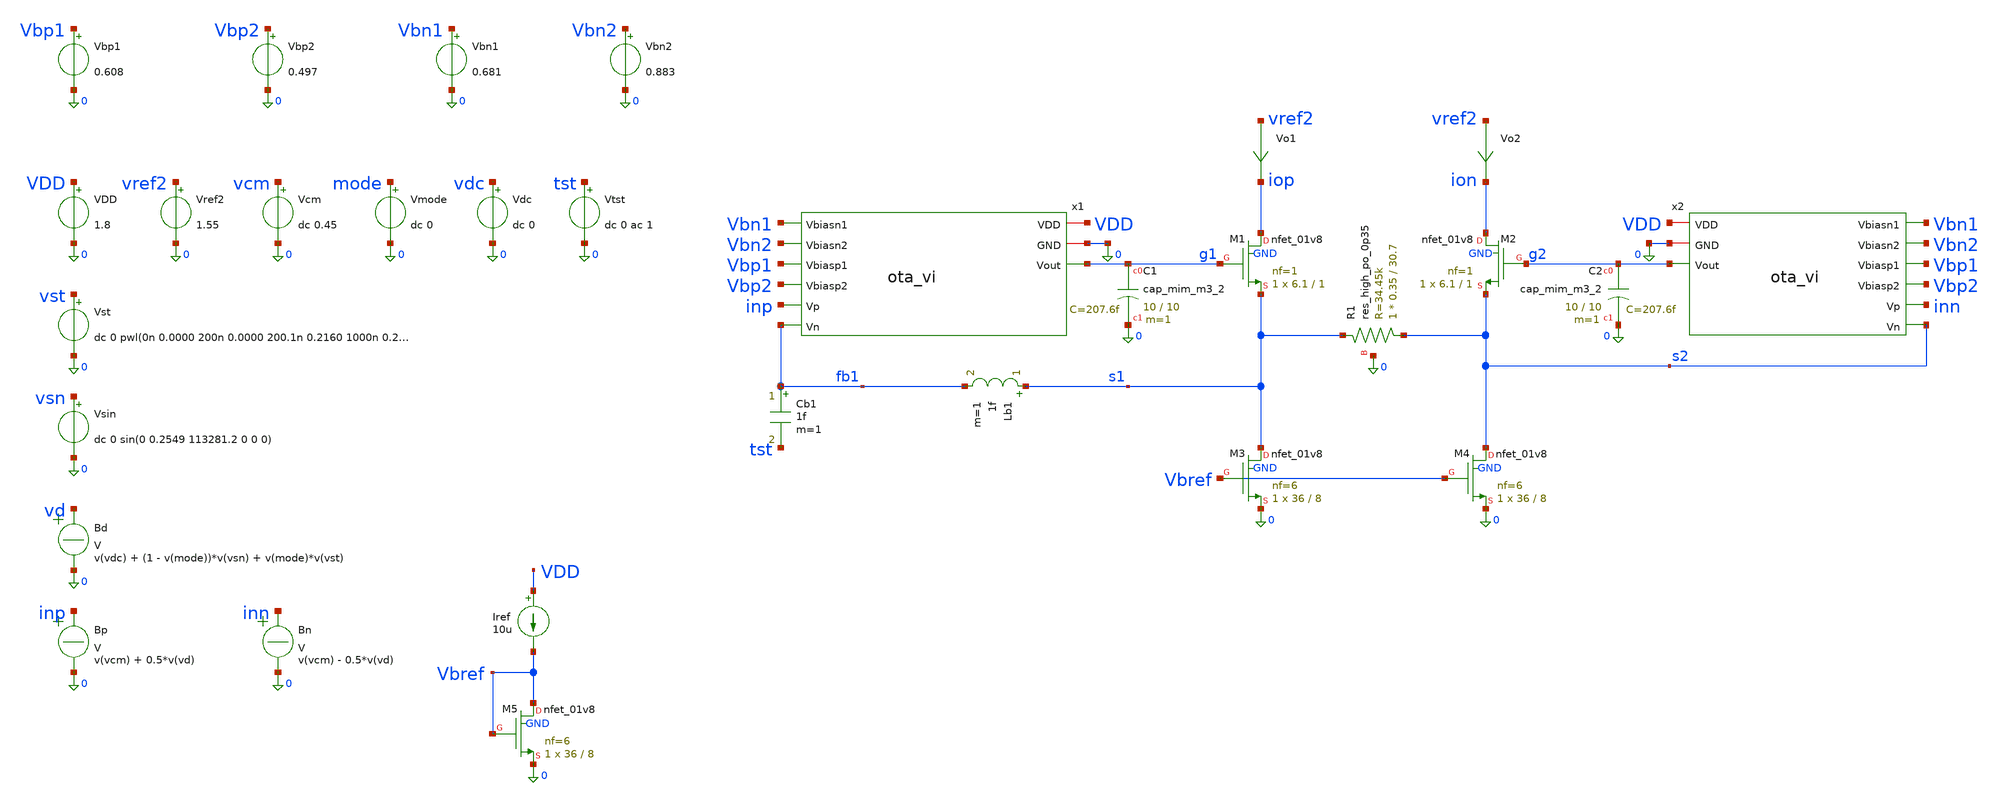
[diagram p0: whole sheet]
** sch_path: sch/vi_converter/vi_converter_tb.sch
**.subckt vi_converter_tb
x1 VDD 0 Vbn1 Vbn2 Vbp1 Vbp2 inp fb1 g1 ota_vi
XM1 iop g1 s1 GND sky130_fd_pr__nfet_01v8 L=1 W=6.1 nf=1 ad='int((1 + 1)/2) * 6.1 / 1 * 0.29' as='int((1 + 2)/2) * 6.1 / 1 * 0.29'
+ pd='2*int((1 + 1)/2) * (6.1 / 1 + 0.29)' ps='2*int((1 + 2)/2) * (6.1 / 1 + 0.29)' nrd='0.29 / 6.1 ' nrs='0.29 / 6.1 '
+ sa=0 sb=0 sd=0 mult=1 m=1
XM2 ion g2 s2 GND sky130_fd_pr__nfet_01v8 L=1 W=6.1 nf=1 ad='int((1 + 1)/2) * 6.1 / 1 * 0.29' as='int((1 + 2)/2) * 6.1 / 1 * 0.29'
+ pd='2*int((1 + 1)/2) * (6.1 / 1 + 0.29)' ps='2*int((1 + 2)/2) * (6.1 / 1 + 0.29)' nrd='0.29 / 6.1 ' nrs='0.29 / 6.1 '
+ sa=0 sb=0 sd=0 mult=1 m=1
XM3 s1 Vbref 0 GND sky130_fd_pr__nfet_01v8 L=8 W=36 nf=6 ad='int((6 + 1)/2) * 36 / 6 * 0.29' as='int((6 + 2)/2) * 36 / 6 * 0.29'
+ pd='2*int((6 + 1)/2) * (36 / 6 + 0.29)' ps='2*int((6 + 2)/2) * (36 / 6 + 0.29)' nrd='0.29 / 36 ' nrs='0.29 / 36 '
+ sa=0 sb=0 sd=0 mult=1 m=1
XM4 s2 Vbref 0 GND sky130_fd_pr__nfet_01v8 L=8 W=36 nf=6 ad='int((6 + 1)/2) * 36 / 6 * 0.29' as='int((6 + 2)/2) * 36 / 6 * 0.29'
+ pd='2*int((6 + 1)/2) * (36 / 6 + 0.29)' ps='2*int((6 + 2)/2) * (36 / 6 + 0.29)' nrd='0.29 / 36 ' nrs='0.29 / 36 '
+ sa=0 sb=0 sd=0 mult=1 m=1
VDD VDD 0 1.8
.save i(vdd)
Iref VDD Vbref 10u
XC1 g1 0 sky130_fd_pr__cap_mim_m3_2 W=10 L=10 MF=1 m=1
x2 VDD 0 Vbn1 Vbn2 Vbp1 Vbp2 inn s2 g2 ota_vi
XC2 g2 0 sky130_fd_pr__cap_mim_m3_2 W=10 L=10 MF=1 m=1
Vref2 vref2 0 1.55
.save i(vref2)
XR1 s2 s1 0 sky130_fd_pr__res_high_po_0p35 L=30.7 mult=1 m=1
Vo1 vref2 iop 0
.save i(vo1)
Vo2 vref2 ion 0
.save i(vo2)
Vcm vcm 0 dc 0.45
.save i(vcm)
Vst vst 0 dc 0 pwl(0n 0.0000 200n 0.0000 200.1n 0.2160 1000n 0.2160 1000.1n -0.2160 1800n -0.2160
+ 1800.1n 0.0000 2600n 0.0000)
.save i(vst)
Bd vd 0 V = v(vdc) + (1 - v(mode))*v(vsn) + v(mode)*v(vst)
Bp inp 0 V = v(vcm) + 0.5*v(vd)
Bn inn 0 V = v(vcm) - 0.5*v(vd)
Vtst tst 0 dc 0 ac 1
.save i(vtst)
Lb1 s1 fb1 1f m=1
Cb1 fb1 tst 1f m=1
Vmode mode 0 dc 0
.save i(vmode)
Vdc vdc 0 dc 0
.save i(vdc)
Vbp2 Vbp2 0 0.497
.save i(vbp2)
Vbp1 Vbp1 0 0.608
.save i(vbp1)
Vbn1 Vbn1 0 0.681
.save i(vbn1)
Vbn2 Vbn2 0 0.883
.save i(vbn2)
XM5 Vbref Vbref 0 GND sky130_fd_pr__nfet_01v8 L=8 W=36 nf=6 ad='int((6 + 1)/2) * 36 / 6 * 0.29' as='int((6 + 2)/2) * 36 / 6 * 0.29'
+ pd='2*int((6 + 1)/2) * (36 / 6 + 0.29)' ps='2*int((6 + 2)/2) * (36 / 6 + 0.29)' nrd='0.29 / 36 ' nrs='0.29 / 36 '
+ sa=0 sb=0 sd=0 mult=1 m=1
Vsin vsn 0 dc 0 sin(0 0.2549 113281.2 0 0 0)
.save i(vsin)
**** begin user architecture code

** opencircuitdesign pdks install
.lib $::SKYWATER_MODELS/sky130.lib.spice tt
.include $::SKYWATER_STDCELLS/sky130_fd_sc_hd.spice



.nodeset v(s1)=0.45 v(s2)=0.45 v(g1)=1.1 v(g2)=1.1
.save all
.option savecurrents
.include vi_converter_tb.save
.control
  save all
  set wr_singlescale
  set wr_vecnames
  * 1. operating points: mid scale, and the two ends of the input range (T1 or T2 nearly off)
  alter Vdc dc = 0
  op
  write @schname\.raw
  let idd = -i(VDD)
  let io1 = i(Vo1)
  let io2 = i(Vo2)
  print idd io1 io2 v(inp) v(inn) v(s1) v(s2) v(g1) v(g2) v(vbref) v(vbp1) v(vbn1) v(vbn2) v(vbp2) >
+ op_mid.log
  print @m.xm1.msky130_fd_pr__nfet_01v8[vds] @m.xm1.msky130_fd_pr__nfet_01v8[vdsat]
+ @m.xm1.msky130_fd_pr__nfet_01v8[gm] @m.xm1.msky130_fd_pr__nfet_01v8[id] >> op_mid.log
  print @m.xm2.msky130_fd_pr__nfet_01v8[vds] @m.xm2.msky130_fd_pr__nfet_01v8[vdsat]
+ @m.xm2.msky130_fd_pr__nfet_01v8[gm] @m.xm2.msky130_fd_pr__nfet_01v8[id] >> op_mid.log
  print @m.xm3.msky130_fd_pr__nfet_01v8[vds] @m.xm3.msky130_fd_pr__nfet_01v8[vdsat]
+ @m.xm3.msky130_fd_pr__nfet_01v8[gm] @m.xm3.msky130_fd_pr__nfet_01v8[id] >> op_mid.log
  print @m.xm4.msky130_fd_pr__nfet_01v8[vds] @m.xm4.msky130_fd_pr__nfet_01v8[vdsat]
+ @m.xm4.msky130_fd_pr__nfet_01v8[gm] @m.xm4.msky130_fd_pr__nfet_01v8[id] >> op_mid.log
  print @m.xm5.msky130_fd_pr__nfet_01v8[vds] @m.xm5.msky130_fd_pr__nfet_01v8[vdsat]
+ @m.xm5.msky130_fd_pr__nfet_01v8[gm] @m.xm5.msky130_fd_pr__nfet_01v8[id] >> op_mid.log
  print @m.x1.xm11.msky130_fd_pr__pfet_01v8[vds] @m.x1.xm11.msky130_fd_pr__pfet_01v8[vdsat]
+ @m.x1.xm11.msky130_fd_pr__pfet_01v8[gm] @m.x1.xm11.msky130_fd_pr__pfet_01v8[id] >> op_mid.log
  print @m.x1.xm1.msky130_fd_pr__pfet_01v8_lvt[vds] @m.x1.xm1.msky130_fd_pr__pfet_01v8_lvt[vdsat]
+ @m.x1.xm1.msky130_fd_pr__pfet_01v8_lvt[gm] @m.x1.xm1.msky130_fd_pr__pfet_01v8_lvt[id] >> op_mid.log
  print @m.x1.xm2.msky130_fd_pr__pfet_01v8_lvt[vds] @m.x1.xm2.msky130_fd_pr__pfet_01v8_lvt[vdsat]
+ @m.x1.xm2.msky130_fd_pr__pfet_01v8_lvt[gm] @m.x1.xm2.msky130_fd_pr__pfet_01v8_lvt[id] >> op_mid.log
  print @m.x1.xm5.msky130_fd_pr__nfet_01v8[vds] @m.x1.xm5.msky130_fd_pr__nfet_01v8[vdsat]
+ @m.x1.xm5.msky130_fd_pr__nfet_01v8[gm] @m.x1.xm5.msky130_fd_pr__nfet_01v8[id] >> op_mid.log
  print @m.x1.xm6.msky130_fd_pr__nfet_01v8[vds] @m.x1.xm6.msky130_fd_pr__nfet_01v8[vdsat]
+ @m.x1.xm6.msky130_fd_pr__nfet_01v8[gm] @m.x1.xm6.msky130_fd_pr__nfet_01v8[id] >> op_mid.log
  print @m.x1.xm3.msky130_fd_pr__nfet_01v8[vds] @m.x1.xm3.msky130_fd_pr__nfet_01v8[vdsat]
+ @m.x1.xm3.msky130_fd_pr__nfet_01v8[gm] @m.x1.xm3.msky130_fd_pr__nfet_01v8[id] >> op_mid.log
  print @m.x1.xm4.msky130_fd_pr__nfet_01v8[vds] @m.x1.xm4.msky130_fd_pr__nfet_01v8[vdsat]
+ @m.x1.xm4.msky130_fd_pr__nfet_01v8[gm] @m.x1.xm4.msky130_fd_pr__nfet_01v8[id] >> op_mid.log
  print @m.x1.xm7.msky130_fd_pr__pfet_01v8[vds] @m.x1.xm7.msky130_fd_pr__pfet_01v8[vdsat]
+ @m.x1.xm7.msky130_fd_pr__pfet_01v8[gm] @m.x1.xm7.msky130_fd_pr__pfet_01v8[id] >> op_mid.log
  print @m.x1.xm8.msky130_fd_pr__pfet_01v8[vds] @m.x1.xm8.msky130_fd_pr__pfet_01v8[vdsat]
+ @m.x1.xm8.msky130_fd_pr__pfet_01v8[gm] @m.x1.xm8.msky130_fd_pr__pfet_01v8[id] >> op_mid.log
  print @m.x1.xm9.msky130_fd_pr__pfet_01v8[vds] @m.x1.xm9.msky130_fd_pr__pfet_01v8[vdsat]
+ @m.x1.xm9.msky130_fd_pr__pfet_01v8[gm] @m.x1.xm9.msky130_fd_pr__pfet_01v8[id] >> op_mid.log
  print @m.x1.xm10.msky130_fd_pr__pfet_01v8[vds] @m.x1.xm10.msky130_fd_pr__pfet_01v8[vdsat]
+ @m.x1.xm10.msky130_fd_pr__pfet_01v8[gm] @m.x1.xm10.msky130_fd_pr__pfet_01v8[id] >> op_mid.log
  print @m.x2.xm11.msky130_fd_pr__pfet_01v8[vds] @m.x2.xm11.msky130_fd_pr__pfet_01v8[vdsat]
+ @m.x2.xm11.msky130_fd_pr__pfet_01v8[gm] @m.x2.xm11.msky130_fd_pr__pfet_01v8[id] >> op_mid.log
  print @m.x2.xm1.msky130_fd_pr__pfet_01v8_lvt[vds] @m.x2.xm1.msky130_fd_pr__pfet_01v8_lvt[vdsat]
+ @m.x2.xm1.msky130_fd_pr__pfet_01v8_lvt[gm] @m.x2.xm1.msky130_fd_pr__pfet_01v8_lvt[id] >> op_mid.log
  print @m.x2.xm2.msky130_fd_pr__pfet_01v8_lvt[vds] @m.x2.xm2.msky130_fd_pr__pfet_01v8_lvt[vdsat]
+ @m.x2.xm2.msky130_fd_pr__pfet_01v8_lvt[gm] @m.x2.xm2.msky130_fd_pr__pfet_01v8_lvt[id] >> op_mid.log
  print @m.x2.xm5.msky130_fd_pr__nfet_01v8[vds] @m.x2.xm5.msky130_fd_pr__nfet_01v8[vdsat]
+ @m.x2.xm5.msky130_fd_pr__nfet_01v8[gm] @m.x2.xm5.msky130_fd_pr__nfet_01v8[id] >> op_mid.log
  print @m.x2.xm6.msky130_fd_pr__nfet_01v8[vds] @m.x2.xm6.msky130_fd_pr__nfet_01v8[vdsat]
+ @m.x2.xm6.msky130_fd_pr__nfet_01v8[gm] @m.x2.xm6.msky130_fd_pr__nfet_01v8[id] >> op_mid.log
  print @m.x2.xm3.msky130_fd_pr__nfet_01v8[vds] @m.x2.xm3.msky130_fd_pr__nfet_01v8[vdsat]
+ @m.x2.xm3.msky130_fd_pr__nfet_01v8[gm] @m.x2.xm3.msky130_fd_pr__nfet_01v8[id] >> op_mid.log
  print @m.x2.xm4.msky130_fd_pr__nfet_01v8[vds] @m.x2.xm4.msky130_fd_pr__nfet_01v8[vdsat]
+ @m.x2.xm4.msky130_fd_pr__nfet_01v8[gm] @m.x2.xm4.msky130_fd_pr__nfet_01v8[id] >> op_mid.log
  print @m.x2.xm7.msky130_fd_pr__pfet_01v8[vds] @m.x2.xm7.msky130_fd_pr__pfet_01v8[vdsat]
+ @m.x2.xm7.msky130_fd_pr__pfet_01v8[gm] @m.x2.xm7.msky130_fd_pr__pfet_01v8[id] >> op_mid.log
  print @m.x2.xm8.msky130_fd_pr__pfet_01v8[vds] @m.x2.xm8.msky130_fd_pr__pfet_01v8[vdsat]
+ @m.x2.xm8.msky130_fd_pr__pfet_01v8[gm] @m.x2.xm8.msky130_fd_pr__pfet_01v8[id] >> op_mid.log
  print @m.x2.xm9.msky130_fd_pr__pfet_01v8[vds] @m.x2.xm9.msky130_fd_pr__pfet_01v8[vdsat]
+ @m.x2.xm9.msky130_fd_pr__pfet_01v8[gm] @m.x2.xm9.msky130_fd_pr__pfet_01v8[id] >> op_mid.log
  print @m.x2.xm10.msky130_fd_pr__pfet_01v8[vds] @m.x2.xm10.msky130_fd_pr__pfet_01v8[vdsat]
+ @m.x2.xm10.msky130_fd_pr__pfet_01v8[gm] @m.x2.xm10.msky130_fd_pr__pfet_01v8[id] >> op_mid.log
  alter Vdc dc = -0.2646
  op
  let idd = -i(VDD)
  let io1 = i(Vo1)
  let io2 = i(Vo2)
  print idd io1 io2 v(inp) v(inn) v(s1) v(s2) v(g1) v(g2) v(vbref) v(vbp1) v(vbn1) v(vbn2) v(vbp2) >
+ op_lo.log
  print @m.xm1.msky130_fd_pr__nfet_01v8[vds] @m.xm1.msky130_fd_pr__nfet_01v8[vdsat]
+ @m.xm1.msky130_fd_pr__nfet_01v8[gm] @m.xm1.msky130_fd_pr__nfet_01v8[id] >> op_lo.log
  print @m.xm2.msky130_fd_pr__nfet_01v8[vds] @m.xm2.msky130_fd_pr__nfet_01v8[vdsat]
+ @m.xm2.msky130_fd_pr__nfet_01v8[gm] @m.xm2.msky130_fd_pr__nfet_01v8[id] >> op_lo.log
  print @m.xm3.msky130_fd_pr__nfet_01v8[vds] @m.xm3.msky130_fd_pr__nfet_01v8[vdsat]
+ @m.xm3.msky130_fd_pr__nfet_01v8[gm] @m.xm3.msky130_fd_pr__nfet_01v8[id] >> op_lo.log
  print @m.xm4.msky130_fd_pr__nfet_01v8[vds] @m.xm4.msky130_fd_pr__nfet_01v8[vdsat]
+ @m.xm4.msky130_fd_pr__nfet_01v8[gm] @m.xm4.msky130_fd_pr__nfet_01v8[id] >> op_lo.log
  print @m.xm5.msky130_fd_pr__nfet_01v8[vds] @m.xm5.msky130_fd_pr__nfet_01v8[vdsat]
+ @m.xm5.msky130_fd_pr__nfet_01v8[gm] @m.xm5.msky130_fd_pr__nfet_01v8[id] >> op_lo.log
  print @m.x1.xm11.msky130_fd_pr__pfet_01v8[vds] @m.x1.xm11.msky130_fd_pr__pfet_01v8[vdsat]
+ @m.x1.xm11.msky130_fd_pr__pfet_01v8[gm] @m.x1.xm11.msky130_fd_pr__pfet_01v8[id] >> op_lo.log
  print @m.x1.xm1.msky130_fd_pr__pfet_01v8_lvt[vds] @m.x1.xm1.msky130_fd_pr__pfet_01v8_lvt[vdsat]
+ @m.x1.xm1.msky130_fd_pr__pfet_01v8_lvt[gm] @m.x1.xm1.msky130_fd_pr__pfet_01v8_lvt[id] >> op_lo.log
  print @m.x1.xm2.msky130_fd_pr__pfet_01v8_lvt[vds] @m.x1.xm2.msky130_fd_pr__pfet_01v8_lvt[vdsat]
+ @m.x1.xm2.msky130_fd_pr__pfet_01v8_lvt[gm] @m.x1.xm2.msky130_fd_pr__pfet_01v8_lvt[id] >> op_lo.log
  print @m.x1.xm5.msky130_fd_pr__nfet_01v8[vds] @m.x1.xm5.msky130_fd_pr__nfet_01v8[vdsat]
+ @m.x1.xm5.msky130_fd_pr__nfet_01v8[gm] @m.x1.xm5.msky130_fd_pr__nfet_01v8[id] >> op_lo.log
  print @m.x1.xm6.msky130_fd_pr__nfet_01v8[vds] @m.x1.xm6.msky130_fd_pr__nfet_01v8[vdsat]
+ @m.x1.xm6.msky130_fd_pr__nfet_01v8[gm] @m.x1.xm6.msky130_fd_pr__nfet_01v8[id] >> op_lo.log
  print @m.x1.xm3.msky130_fd_pr__nfet_01v8[vds] @m.x1.xm3.msky130_fd_pr__nfet_01v8[vdsat]
+ @m.x1.xm3.msky130_fd_pr__nfet_01v8[gm] @m.x1.xm3.msky130_fd_pr__nfet_01v8[id] >> op_lo.log
  print @m.x1.xm4.msky130_fd_pr__nfet_01v8[vds] @m.x1.xm4.msky130_fd_pr__nfet_01v8[vdsat]
+ @m.x1.xm4.msky130_fd_pr__nfet_01v8[gm] @m.x1.xm4.msky130_fd_pr__nfet_01v8[id] >> op_lo.log
  print @m.x1.xm7.msky130_fd_pr__pfet_01v8[vds] @m.x1.xm7.msky130_fd_pr__pfet_01v8[vdsat]
+ @m.x1.xm7.msky130_fd_pr__pfet_01v8[gm] @m.x1.xm7.msky130_fd_pr__pfet_01v8[id] >> op_lo.log
  print @m.x1.xm8.msky130_fd_pr__pfet_01v8[vds] @m.x1.xm8.msky130_fd_pr__pfet_01v8[vdsat]
+ @m.x1.xm8.msky130_fd_pr__pfet_01v8[gm] @m.x1.xm8.msky130_fd_pr__pfet_01v8[id] >> op_lo.log
  print @m.x1.xm9.msky130_fd_pr__pfet_01v8[vds] @m.x1.xm9.msky130_fd_pr__pfet_01v8[vdsat]
+ @m.x1.xm9.msky130_fd_pr__pfet_01v8[gm] @m.x1.xm9.msky130_fd_pr__pfet_01v8[id] >> op_lo.log
  print @m.x1.xm10.msky130_fd_pr__pfet_01v8[vds] @m.x1.xm10.msky130_fd_pr__pfet_01v8[vdsat]
+ @m.x1.xm10.msky130_fd_pr__pfet_01v8[gm] @m.x1.xm10.msky130_fd_pr__pfet_01v8[id] >> op_lo.log
  print @m.x2.xm11.msky130_fd_pr__pfet_01v8[vds] @m.x2.xm11.msky130_fd_pr__pfet_01v8[vdsat]
+ @m.x2.xm11.msky130_fd_pr__pfet_01v8[gm] @m.x2.xm11.msky130_fd_pr__pfet_01v8[id] >> op_lo.log
  print @m.x2.xm1.msky130_fd_pr__pfet_01v8_lvt[vds] @m.x2.xm1.msky130_fd_pr__pfet_01v8_lvt[vdsat]
+ @m.x2.xm1.msky130_fd_pr__pfet_01v8_lvt[gm] @m.x2.xm1.msky130_fd_pr__pfet_01v8_lvt[id] >> op_lo.log
  print @m.x2.xm2.msky130_fd_pr__pfet_01v8_lvt[vds] @m.x2.xm2.msky130_fd_pr__pfet_01v8_lvt[vdsat]
+ @m.x2.xm2.msky130_fd_pr__pfet_01v8_lvt[gm] @m.x2.xm2.msky130_fd_pr__pfet_01v8_lvt[id] >> op_lo.log
  print @m.x2.xm5.msky130_fd_pr__nfet_01v8[vds] @m.x2.xm5.msky130_fd_pr__nfet_01v8[vdsat]
+ @m.x2.xm5.msky130_fd_pr__nfet_01v8[gm] @m.x2.xm5.msky130_fd_pr__nfet_01v8[id] >> op_lo.log
  print @m.x2.xm6.msky130_fd_pr__nfet_01v8[vds] @m.x2.xm6.msky130_fd_pr__nfet_01v8[vdsat]
+ @m.x2.xm6.msky130_fd_pr__nfet_01v8[gm] @m.x2.xm6.msky130_fd_pr__nfet_01v8[id] >> op_lo.log
  print @m.x2.xm3.msky130_fd_pr__nfet_01v8[vds] @m.x2.xm3.msky130_fd_pr__nfet_01v8[vdsat]
+ @m.x2.xm3.msky130_fd_pr__nfet_01v8[gm] @m.x2.xm3.msky130_fd_pr__nfet_01v8[id] >> op_lo.log
  print @m.x2.xm4.msky130_fd_pr__nfet_01v8[vds] @m.x2.xm4.msky130_fd_pr__nfet_01v8[vdsat]
+ @m.x2.xm4.msky130_fd_pr__nfet_01v8[gm] @m.x2.xm4.msky130_fd_pr__nfet_01v8[id] >> op_lo.log
  print @m.x2.xm7.msky130_fd_pr__pfet_01v8[vds] @m.x2.xm7.msky130_fd_pr__pfet_01v8[vdsat]
+ @m.x2.xm7.msky130_fd_pr__pfet_01v8[gm] @m.x2.xm7.msky130_fd_pr__pfet_01v8[id] >> op_lo.log
  print @m.x2.xm8.msky130_fd_pr__pfet_01v8[vds] @m.x2.xm8.msky130_fd_pr__pfet_01v8[vdsat]
+ @m.x2.xm8.msky130_fd_pr__pfet_01v8[gm] @m.x2.xm8.msky130_fd_pr__pfet_01v8[id] >> op_lo.log
  print @m.x2.xm9.msky130_fd_pr__pfet_01v8[vds] @m.x2.xm9.msky130_fd_pr__pfet_01v8[vdsat]
+ @m.x2.xm9.msky130_fd_pr__pfet_01v8[gm] @m.x2.xm9.msky130_fd_pr__pfet_01v8[id] >> op_lo.log
  print @m.x2.xm10.msky130_fd_pr__pfet_01v8[vds] @m.x2.xm10.msky130_fd_pr__pfet_01v8[vdsat]
+ @m.x2.xm10.msky130_fd_pr__pfet_01v8[gm] @m.x2.xm10.msky130_fd_pr__pfet_01v8[id] >> op_lo.log
  alter Vdc dc = 0.2646
  op
  let idd = -i(VDD)
  let io1 = i(Vo1)
  let io2 = i(Vo2)
  print idd io1 io2 v(inp) v(inn) v(s1) v(s2) v(g1) v(g2) v(vbref) v(vbp1) v(vbn1) v(vbn2) v(vbp2) >
+ op_hi.log
  print @m.xm1.msky130_fd_pr__nfet_01v8[vds] @m.xm1.msky130_fd_pr__nfet_01v8[vdsat]
+ @m.xm1.msky130_fd_pr__nfet_01v8[gm] @m.xm1.msky130_fd_pr__nfet_01v8[id] >> op_hi.log
  print @m.xm2.msky130_fd_pr__nfet_01v8[vds] @m.xm2.msky130_fd_pr__nfet_01v8[vdsat]
+ @m.xm2.msky130_fd_pr__nfet_01v8[gm] @m.xm2.msky130_fd_pr__nfet_01v8[id] >> op_hi.log
  print @m.xm3.msky130_fd_pr__nfet_01v8[vds] @m.xm3.msky130_fd_pr__nfet_01v8[vdsat]
+ @m.xm3.msky130_fd_pr__nfet_01v8[gm] @m.xm3.msky130_fd_pr__nfet_01v8[id] >> op_hi.log
  print @m.xm4.msky130_fd_pr__nfet_01v8[vds] @m.xm4.msky130_fd_pr__nfet_01v8[vdsat]
+ @m.xm4.msky130_fd_pr__nfet_01v8[gm] @m.xm4.msky130_fd_pr__nfet_01v8[id] >> op_hi.log
  print @m.xm5.msky130_fd_pr__nfet_01v8[vds] @m.xm5.msky130_fd_pr__nfet_01v8[vdsat]
+ @m.xm5.msky130_fd_pr__nfet_01v8[gm] @m.xm5.msky130_fd_pr__nfet_01v8[id] >> op_hi.log
  print @m.x1.xm11.msky130_fd_pr__pfet_01v8[vds] @m.x1.xm11.msky130_fd_pr__pfet_01v8[vdsat]
+ @m.x1.xm11.msky130_fd_pr__pfet_01v8[gm] @m.x1.xm11.msky130_fd_pr__pfet_01v8[id] >> op_hi.log
  print @m.x1.xm1.msky130_fd_pr__pfet_01v8_lvt[vds] @m.x1.xm1.msky130_fd_pr__pfet_01v8_lvt[vdsat]
+ @m.x1.xm1.msky130_fd_pr__pfet_01v8_lvt[gm] @m.x1.xm1.msky130_fd_pr__pfet_01v8_lvt[id] >> op_hi.log
  print @m.x1.xm2.msky130_fd_pr__pfet_01v8_lvt[vds] @m.x1.xm2.msky130_fd_pr__pfet_01v8_lvt[vdsat]
+ @m.x1.xm2.msky130_fd_pr__pfet_01v8_lvt[gm] @m.x1.xm2.msky130_fd_pr__pfet_01v8_lvt[id] >> op_hi.log
  print @m.x1.xm5.msky130_fd_pr__nfet_01v8[vds] @m.x1.xm5.msky130_fd_pr__nfet_01v8[vdsat]
+ @m.x1.xm5.msky130_fd_pr__nfet_01v8[gm] @m.x1.xm5.msky130_fd_pr__nfet_01v8[id] >> op_hi.log
  print @m.x1.xm6.msky130_fd_pr__nfet_01v8[vds] @m.x1.xm6.msky130_fd_pr__nfet_01v8[vdsat]
+ @m.x1.xm6.msky130_fd_pr__nfet_01v8[gm] @m.x1.xm6.msky130_fd_pr__nfet_01v8[id] >> op_hi.log
  print @m.x1.xm3.msky130_fd_pr__nfet_01v8[vds] @m.x1.xm3.msky130_fd_pr__nfet_01v8[vdsat]
+ @m.x1.xm3.msky130_fd_pr__nfet_01v8[gm] @m.x1.xm3.msky130_fd_pr__nfet_01v8[id] >> op_hi.log
  print @m.x1.xm4.msky130_fd_pr__nfet_01v8[vds] @m.x1.xm4.msky130_fd_pr__nfet_01v8[vdsat]
+ @m.x1.xm4.msky130_fd_pr__nfet_01v8[gm] @m.x1.xm4.msky130_fd_pr__nfet_01v8[id] >> op_hi.log
  print @m.x1.xm7.msky130_fd_pr__pfet_01v8[vds] @m.x1.xm7.msky130_fd_pr__pfet_01v8[vdsat]
+ @m.x1.xm7.msky130_fd_pr__pfet_01v8[gm] @m.x1.xm7.msky130_fd_pr__pfet_01v8[id] >> op_hi.log
  print @m.x1.xm8.msky130_fd_pr__pfet_01v8[vds] @m.x1.xm8.msky130_fd_pr__pfet_01v8[vdsat]
+ @m.x1.xm8.msky130_fd_pr__pfet_01v8[gm] @m.x1.xm8.msky130_fd_pr__pfet_01v8[id] >> op_hi.log
  print @m.x1.xm9.msky130_fd_pr__pfet_01v8[vds] @m.x1.xm9.msky130_fd_pr__pfet_01v8[vdsat]
+ @m.x1.xm9.msky130_fd_pr__pfet_01v8[gm] @m.x1.xm9.msky130_fd_pr__pfet_01v8[id] >> op_hi.log
  print @m.x1.xm10.msky130_fd_pr__pfet_01v8[vds] @m.x1.xm10.msky130_fd_pr__pfet_01v8[vdsat]
+ @m.x1.xm10.msky130_fd_pr__pfet_01v8[gm] @m.x1.xm10.msky130_fd_pr__pfet_01v8[id] >> op_hi.log
  print @m.x2.xm11.msky130_fd_pr__pfet_01v8[vds] @m.x2.xm11.msky130_fd_pr__pfet_01v8[vdsat]
+ @m.x2.xm11.msky130_fd_pr__pfet_01v8[gm] @m.x2.xm11.msky130_fd_pr__pfet_01v8[id] >> op_hi.log
  print @m.x2.xm1.msky130_fd_pr__pfet_01v8_lvt[vds] @m.x2.xm1.msky130_fd_pr__pfet_01v8_lvt[vdsat]
+ @m.x2.xm1.msky130_fd_pr__pfet_01v8_lvt[gm] @m.x2.xm1.msky130_fd_pr__pfet_01v8_lvt[id] >> op_hi.log
  print @m.x2.xm2.msky130_fd_pr__pfet_01v8_lvt[vds] @m.x2.xm2.msky130_fd_pr__pfet_01v8_lvt[vdsat]
+ @m.x2.xm2.msky130_fd_pr__pfet_01v8_lvt[gm] @m.x2.xm2.msky130_fd_pr__pfet_01v8_lvt[id] >> op_hi.log
  print @m.x2.xm5.msky130_fd_pr__nfet_01v8[vds] @m.x2.xm5.msky130_fd_pr__nfet_01v8[vdsat]
+ @m.x2.xm5.msky130_fd_pr__nfet_01v8[gm] @m.x2.xm5.msky130_fd_pr__nfet_01v8[id] >> op_hi.log
  print @m.x2.xm6.msky130_fd_pr__nfet_01v8[vds] @m.x2.xm6.msky130_fd_pr__nfet_01v8[vdsat]
+ @m.x2.xm6.msky130_fd_pr__nfet_01v8[gm] @m.x2.xm6.msky130_fd_pr__nfet_01v8[id] >> op_hi.log
  print @m.x2.xm3.msky130_fd_pr__nfet_01v8[vds] @m.x2.xm3.msky130_fd_pr__nfet_01v8[vdsat]
+ @m.x2.xm3.msky130_fd_pr__nfet_01v8[gm] @m.x2.xm3.msky130_fd_pr__nfet_01v8[id] >> op_hi.log
  print @m.x2.xm4.msky130_fd_pr__nfet_01v8[vds] @m.x2.xm4.msky130_fd_pr__nfet_01v8[vdsat]
+ @m.x2.xm4.msky130_fd_pr__nfet_01v8[gm] @m.x2.xm4.msky130_fd_pr__nfet_01v8[id] >> op_hi.log
  print @m.x2.xm7.msky130_fd_pr__pfet_01v8[vds] @m.x2.xm7.msky130_fd_pr__pfet_01v8[vdsat]
+ @m.x2.xm7.msky130_fd_pr__pfet_01v8[gm] @m.x2.xm7.msky130_fd_pr__pfet_01v8[id] >> op_hi.log
  print @m.x2.xm8.msky130_fd_pr__pfet_01v8[vds] @m.x2.xm8.msky130_fd_pr__pfet_01v8[vdsat]
+ @m.x2.xm8.msky130_fd_pr__pfet_01v8[gm] @m.x2.xm8.msky130_fd_pr__pfet_01v8[id] >> op_hi.log
  print @m.x2.xm9.msky130_fd_pr__pfet_01v8[vds] @m.x2.xm9.msky130_fd_pr__pfet_01v8[vdsat]
+ @m.x2.xm9.msky130_fd_pr__pfet_01v8[gm] @m.x2.xm9.msky130_fd_pr__pfet_01v8[id] >> op_hi.log
  print @m.x2.xm10.msky130_fd_pr__pfet_01v8[vds] @m.x2.xm10.msky130_fd_pr__pfet_01v8[vdsat]
+ @m.x2.xm10.msky130_fd_pr__pfet_01v8[gm] @m.x2.xm10.msky130_fd_pr__pfet_01v8[id] >> op_hi.log
  alter Vdc dc = 0

  * 2. static transfer: vd from -(half + 0.05) to +(half + 0.05)
  dc Vdc -0.350 0.350 0.002
  let io1 = i(Vo1)
  let io2 = i(Vo2)
  let vs1 = v(s1)
  let vs2 = v(s2)
  let vg1 = v(g1)
  let vg2 = v(g2)
  let vinp = v(inp)
  let vinn = v(inn)
  let idd = -i(VDD)
  wrdata dc_sweep.csv io1 io2 vs1 vs2 vg1 vg2 vinp vinn idd

  * 3. input common-mode sweeps at three differential inputs
  alter Vdc dc = -0.243
  dc Vcm 0.05 1.45 0.01
  let io1 = i(Vo1)
  let io2 = i(Vo2)
  let vs1 = v(s1)
  let vs2 = v(s2)
  let vg1 = v(g1)
  let vg2 = v(g2)
  let vinp = v(inp)
  let vinn = v(inn)
  let idd = -i(VDD)
  wrdata cm_sweep_lo.csv io1 io2 vs1 vs2 vg1 vg2 vinp vinn idd
  alter Vdc dc = 0
  dc Vcm 0.05 1.45 0.01
  let io1 = i(Vo1)
  let io2 = i(Vo2)
  let vs1 = v(s1)
  let vs2 = v(s2)
  let vg1 = v(g1)
  let vg2 = v(g2)
  let vinp = v(inp)
  let vinn = v(inn)
  let idd = -i(VDD)
  wrdata cm_sweep_mid.csv io1 io2 vs1 vs2 vg1 vg2 vinp vinn idd
  alter Vdc dc = 0.243
  dc Vcm 0.05 1.45 0.01
  let io1 = i(Vo1)
  let io2 = i(Vo2)
  let vs1 = v(s1)
  let vs2 = v(s2)
  let vg1 = v(g1)
  let vg2 = v(g2)
  let vinp = v(inp)
  let vinn = v(inn)
  let idd = -i(VDD)
  wrdata cm_sweep_hi.csv io1 io2 vs1 vs2 vg1 vg2 vinp vinn idd
  alter Vdc dc = 0

  * 4. voltage of the regulated nodes (where do T1 and T2 stay saturated?)
  dc Vref2 0.3 1.8 0.01
  let io1 = i(Vo1)
  let io2 = i(Vo2)
  let vs1 = v(s1)
  let vs2 = v(s2)
  let vg1 = v(g1)
  let vg2 = v(g2)
  let vinp = v(inp)
  let vinn = v(inn)
  let idd = -i(VDD)
  wrdata out_sweep.csv io1 io2 vs1 vs2 vg1 vg2 vinp vinn idd
  alter Vref2 dc = 1.55

  * 5. transient with the coherent sine (-0.5 dBFS, 113.28 kHz, 29 periods in 256 us)
  alter Vmode dc = 0
  option reltol=1e-4
  tran 5n 256.0u
  let vdiff = v(inp) - v(inn)
  let io1 = i(Vo1)
  let io2 = i(Vo2)
  wrdata tran_sine.csv vdiff io1 io2

  * 6. transient with large steps (settling): 0 -> +0.8 half -> -0.8 half -> 0
  alter Vmode dc = 1
  tran 0.1n 2.6u
  let vdiff = v(inp) - v(inn)
  let io1 = i(Vo1)
  let io2 = i(Vo2)
  let vg1 = v(g1)
  let vs1 = v(s1)
  wrdata tran_step.csv vdiff io1 io2 vg1 vs1

  * 7. loop gain of side 1: open the feedback into OTA 1 (1 GH from s1 to fb1) and feed the test
+ signal in through 1 GF at tst.
  *    T(s) = - v(s1) / v(fb1); v(fb1) is the test signal itself. Mid scale and the two ends of the
+ range.
  alter Vdc dc = 0
  alter Lb1 = 1G
  alter Cb1 = 1G
  op
  ac dec 40 1k 10G
  let lg = -v(s1)
  wrdata ac_loop_mid.csv lg
  alter Vdc dc = -0.243
  op
  ac dec 40 1k 10G
  let lg = -v(s1)
  wrdata ac_loop_lo.csv lg
  alter Vdc dc = 0.243
  op
  ac dec 40 1k 10G
  let lg = -v(s1)
  wrdata ac_loop_hi.csv lg
  alter Lb1 = 1p
  alter Cb1 = 1f
  alter Vdc dc = 0
.endc


**** end user architecture code
**.ends

* expanding   symbol:  vi_converter/ota_vi.sym # of pins=9
** sym_path: sch/vi_converter/ota_vi.sym
** sch_path: sch/vi_converter/ota_vi.sch
.subckt ota_vi VDD GND Vbiasn1 Vbiasn2 Vbiasp1 Vbiasp2 Vp Vn Vout
*.ipin Vbiasn2
*.opin Vout
*.iopin VDD
*.iopin GND
*.ipin Vp
*.ipin Vn
*.ipin Vbiasp1
*.ipin Vbiasp2
*.ipin Vbiasn1
XM3 net4 Vbiasn2 net3 GND sky130_fd_pr__nfet_01v8 L=1 W=4.6 nf=1 ad='int((1 + 1)/2) * 4.6 / 1 * 0.29'
+ as='int((1 + 2)/2) * 4.6 / 1 * 0.29' pd='2*int((1 + 1)/2) * (4.6 / 1 + 0.29)' ps='2*int((1 + 2)/2) * (4.6 / 1 + 0.29)'
+ nrd='0.29 / 4.6 ' nrs='0.29 / 4.6 ' sa=0 sb=0 sd=0 mult=1 m=1
XM4 Vout Vbiasn2 net2 GND sky130_fd_pr__nfet_01v8 L=1 W=4.6 nf=1 ad='int((1 + 1)/2) * 4.6 / 1 * 0.29'
+ as='int((1 + 2)/2) * 4.6 / 1 * 0.29' pd='2*int((1 + 1)/2) * (4.6 / 1 + 0.29)' ps='2*int((1 + 2)/2) * (4.6 / 1 + 0.29)'
+ nrd='0.29 / 4.6 ' nrs='0.29 / 4.6 ' sa=0 sb=0 sd=0 mult=1 m=1
XM5 net3 Vbiasn1 GND GND sky130_fd_pr__nfet_01v8 L=2 W=12 nf=2 ad='int((2 + 1)/2) * 12 / 2 * 0.29' as='int((2 + 2)/2) * 12 / 2 * 0.29'
+ pd='2*int((2 + 1)/2) * (12 / 2 + 0.29)' ps='2*int((2 + 2)/2) * (12 / 2 + 0.29)' nrd='0.29 / 12 ' nrs='0.29 / 12 '
+ sa=0 sb=0 sd=0 mult=1 m=1
XM6 net2 Vbiasn1 GND GND sky130_fd_pr__nfet_01v8 L=2 W=12 nf=2 ad='int((2 + 1)/2) * 12 / 2 * 0.29' as='int((2 + 2)/2) * 12 / 2 * 0.29'
+ pd='2*int((2 + 1)/2) * (12 / 2 + 0.29)' ps='2*int((2 + 2)/2) * (12 / 2 + 0.29)' nrd='0.29 / 12 ' nrs='0.29 / 12 '
+ sa=0 sb=0 sd=0 mult=1 m=1
XM7 net4 Vbiasp2 net5 VDD sky130_fd_pr__pfet_01v8 L=1 W=15.6 nf=3 ad='int((3 + 1)/2) * 15.6 / 3 * 0.29'
+ as='int((3 + 2)/2) * 15.6 / 3 * 0.29' pd='2*int((3 + 1)/2) * (15.6 / 3 + 0.29)' ps='2*int((3 + 2)/2) * (15.6 / 3 + 0.29)'
+ nrd='0.29 / 15.6 ' nrs='0.29 / 15.6 ' sa=0 sb=0 sd=0 mult=1 m=1
XM8 Vout Vbiasp2 net6 VDD sky130_fd_pr__pfet_01v8 L=1 W=15.6 nf=3 ad='int((3 + 1)/2) * 15.6 / 3 * 0.29'
+ as='int((3 + 2)/2) * 15.6 / 3 * 0.29' pd='2*int((3 + 1)/2) * (15.6 / 3 + 0.29)' ps='2*int((3 + 2)/2) * (15.6 / 3 + 0.29)'
+ nrd='0.29 / 15.6 ' nrs='0.29 / 15.6 ' sa=0 sb=0 sd=0 mult=1 m=1
XM9 net5 net4 VDD VDD sky130_fd_pr__pfet_01v8 L=2 W=22.6 nf=4 ad='int((4 + 1)/2) * 22.6 / 4 * 0.29' as='int((4 + 2)/2) * 22.6 / 4 * 0.29'
+ pd='2*int((4 + 1)/2) * (22.6 / 4 + 0.29)' ps='2*int((4 + 2)/2) * (22.6 / 4 + 0.29)' nrd='0.29 / 22.6 '
+ nrs='0.29 / 22.6 ' sa=0 sb=0 sd=0 mult=1 m=1
XM10 net6 net4 VDD VDD sky130_fd_pr__pfet_01v8 L=2 W=22.6 nf=4 ad='int((4 + 1)/2) * 22.6 / 4 * 0.29'
+ as='int((4 + 2)/2) * 22.6 / 4 * 0.29' pd='2*int((4 + 1)/2) * (22.6 / 4 + 0.29)' ps='2*int((4 + 2)/2) * (22.6 / 4 + 0.29)'
+ nrd='0.29 / 22.6 ' nrs='0.29 / 22.6 ' sa=0 sb=0 sd=0 mult=1 m=1
XM11 net1 Vbiasp1 VDD VDD sky130_fd_pr__pfet_01v8 L=2 W=17.7 nf=3 ad='int((3 + 1)/2) * 17.7 / 3 * 0.29'
+ as='int((3 + 2)/2) * 17.7 / 3 * 0.29' pd='2*int((3 + 1)/2) * (17.7 / 3 + 0.29)' ps='2*int((3 + 2)/2) * (17.7 / 3 + 0.29)'
+ nrd='0.29 / 17.7 ' nrs='0.29 / 17.7 ' sa=0 sb=0 sd=0 mult=1 m=1
XM1 net3 Vp net1 VDD sky130_fd_pr__pfet_01v8_lvt L=1 W=14.6 nf=2 ad='int((2 + 1)/2) * 14.6 / 2 * 0.29'
+ as='int((2 + 2)/2) * 14.6 / 2 * 0.29' pd='2*int((2 + 1)/2) * (14.6 / 2 + 0.29)' ps='2*int((2 + 2)/2) * (14.6 / 2 + 0.29)'
+ nrd='0.29 / 14.6 ' nrs='0.29 / 14.6 ' sa=0 sb=0 sd=0 mult=1 m=1
XM2 net2 Vn net1 VDD sky130_fd_pr__pfet_01v8_lvt L=1 W=14.6 nf=2 ad='int((2 + 1)/2) * 14.6 / 2 * 0.29'
+ as='int((2 + 2)/2) * 14.6 / 2 * 0.29' pd='2*int((2 + 1)/2) * (14.6 / 2 + 0.29)' ps='2*int((2 + 2)/2) * (14.6 / 2 + 0.29)'
+ nrd='0.29 / 14.6 ' nrs='0.29 / 14.6 ' sa=0 sb=0 sd=0 mult=1 m=1
.ends

.end
